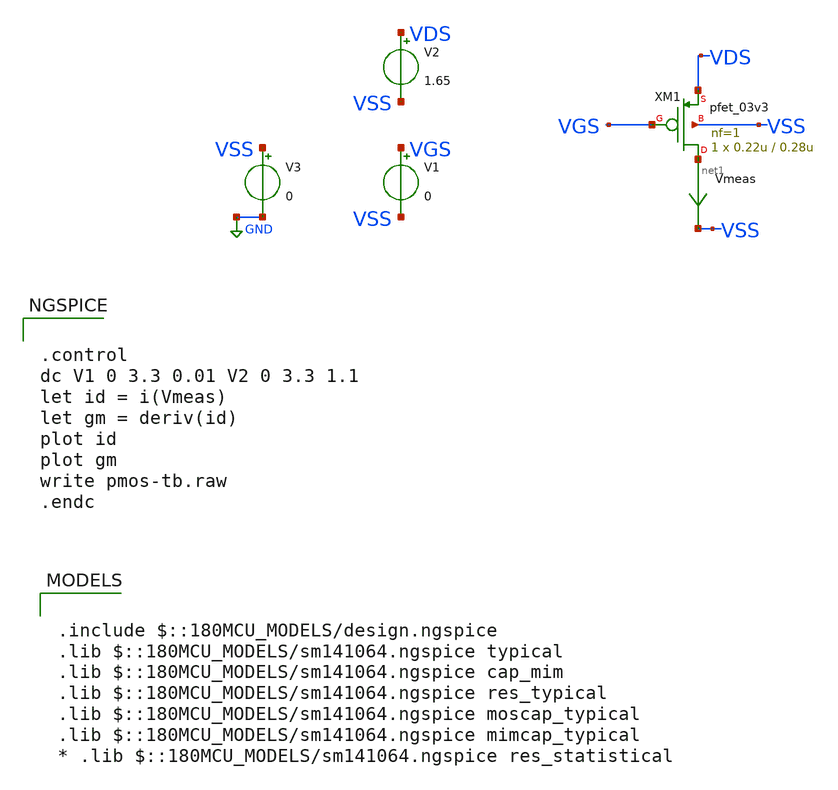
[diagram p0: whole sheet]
** sch_path: w1_advanced-foundation/w1_task/w1_current_mirror/pmos-tb.sch
**.subckt pmos-tb
V1 VGS VSS 0
V2 VDS VSS 1.65
XM1 net1 VGS VDS VSS pfet_03v3 L=0.28u W=0.22u nf=1 ad='int((nf+1)/2) * W/nf * 0.18u' as='int((nf+2)/2) * W/nf * 0.18u'
+ pd='2*int((nf+1)/2) * (W/nf + 0.18u)' ps='2*int((nf+2)/2) * (W/nf + 0.18u)' nrd='0.18u / W' nrs='0.18u / W'
+ sa=0 sb=0 sd=0 m=1
V3 VSS net2 0
Vmeas net1 VSS 0
.save i(vmeas)
**** begin user architecture code

.include $::180MCU_MODELS/design.ngspice
.lib $::180MCU_MODELS/sm141064.ngspice typical
.lib $::180MCU_MODELS/sm141064.ngspice cap_mim
.lib $::180MCU_MODELS/sm141064.ngspice res_typical
.lib $::180MCU_MODELS/sm141064.ngspice moscap_typical
.lib $::180MCU_MODELS/sm141064.ngspice mimcap_typical
* .lib $::180MCU_MODELS/sm141064.ngspice res_statistical



.control
dc V1 0 3.3 0.01 V2 0 3.3 1.1
let id = i(Vmeas)
let gm = deriv(id)
plot id
plot gm
write pmos-tb.raw
.endc


**** end user architecture code
**.ends
.GLOBAL GND
.end
